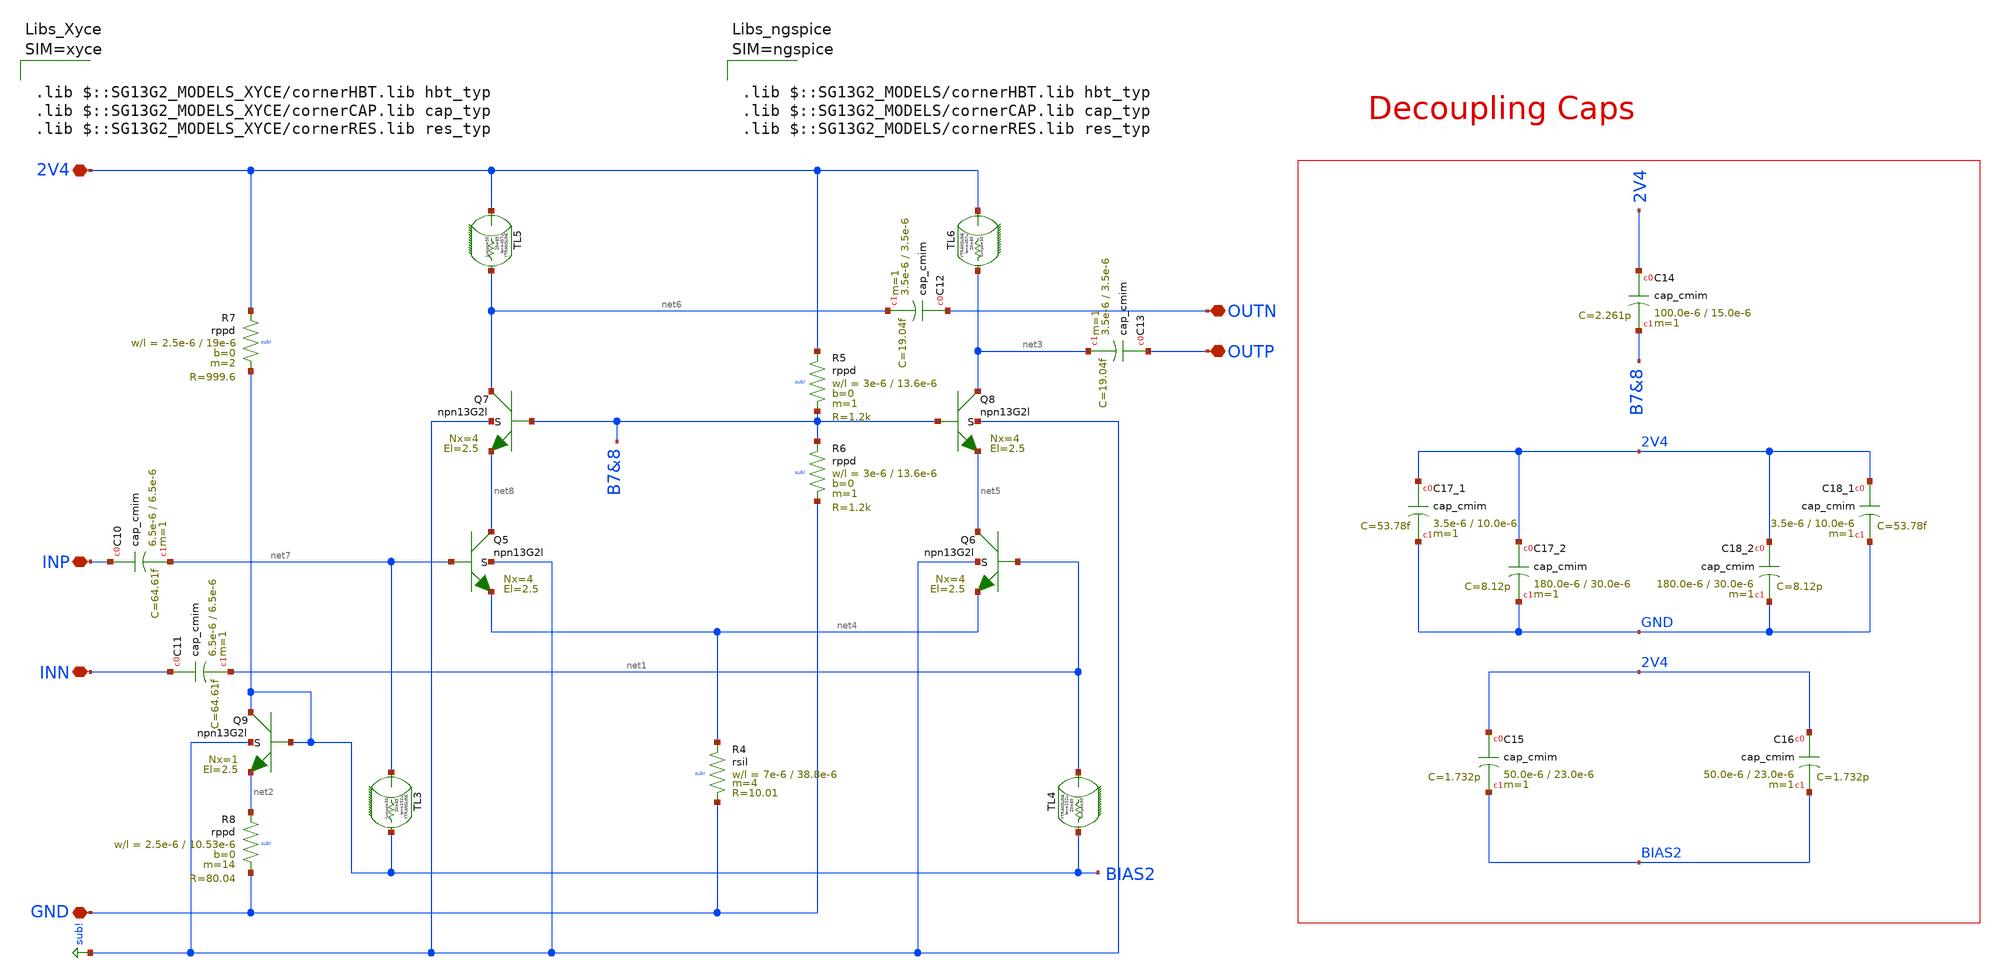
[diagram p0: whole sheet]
** sch_path: mWATTBAT/design_data/xschem/RFAMP_50GD.sch
**.subckt RFAMP_50GD 2V4 GND OUTN OUTP INP INN
*.iopin 2V4
*.iopin GND
*.iopin OUTN
*.iopin OUTP
*.iopin INP
*.iopin INN
XQ5 net8 net7 net4 sub! npn13G2l Nx=4 El=2.5 mm_ok=1
XQ6 net5 net1 net4 sub! npn13G2l Nx=4 El=2.5 mm_ok=1
XQ9 BIAS2 BIAS2 net2 sub! npn13G2l Nx=1 El=2.5 mm_ok=1
XQ7 net6 B7&8 net8 sub! npn13G2l Nx=4 El=2.5 mm_ok=1
XQ8 net3 B7&8 net5 sub! npn13G2l Nx=4 El=2.5 mm_ok=1
ytransline TL5 2V4 net6 ytransline_TL5 len=457u lumps=50
.model ytransline_TL5 transline r=13.18k l=445.8n C=61.5p
ytransline TL6 2V4 net3 ytransline_TL6 len=457u lumps=50
.model ytransline_TL6 transline r=13.18k l=445.8n C=61.5p
ytransline TL3 net7 BIAS2 ytransline_TL3 len=152u lumps=50
.model ytransline_TL3 transline r=13.18k l=445.8n C=61.5p
ytransline TL4 net1 BIAS2 ytransline_TL4 len=152u lumps=50
.model ytransline_TL4 transline r=13.18k l=445.8n C=61.5p
XR7 2V4 BIAS2 sub! rppd w=2.5e-6 l=19e-6 m=2 b=0 mm_ok=1
XC10 INP net7 cap_cmim w=6.5e-6 l=6.5e-6 m=1 mm_ok=1
XC11 INN net1 cap_cmim w=6.5e-6 l=6.5e-6 m=1 mm_ok=1
XC12 OUTN net6 cap_cmim w=3.5e-6 l=3.5e-6 m=1 mm_ok=1
XC13 OUTP net3 cap_cmim w=3.5e-6 l=3.5e-6 m=1 mm_ok=1
XC14 2V4 B7&8 cap_cmim w=100.0e-6 l=15.0e-6 m=1 mm_ok=1
XC15 2V4 BIAS2 cap_cmim w=50.0e-6 l=23.0e-6 m=1 mm_ok=1
XC16 2V4 BIAS2 cap_cmim w=50.0e-6 l=23.0e-6 m=1 mm_ok=1
XC17_1 2V4 GND cap_cmim w=3.5e-6 l=10.0e-6 m=1 mm_ok=1
XC17_2 2V4 GND cap_cmim w=180.0e-6 l=30.0e-6 m=1 mm_ok=1
XC18_1 2V4 GND cap_cmim w=3.5e-6 l=10.0e-6 m=1 mm_ok=1
XC18_2 2V4 GND cap_cmim w=180.0e-6 l=30.0e-6 m=1 mm_ok=1
XR6 B7&8 GND sub! rppd w=3e-6 l=13.6e-6 m=1 b=0 mm_ok=1
XR5 2V4 B7&8 sub! rppd w=3e-6 l=13.6e-6 m=1 b=0 mm_ok=1
XR8 net2 GND sub! rppd w=2.5e-6 l=10.53e-6 m=14 b=0 mm_ok=1
XR4 net4 GND sub! rsil w=7e-6 l=38.8e-6 m=4 mm_ok=1
**** begin user architecture code






.lib $::SG13G2_MODELS/cornerHBT.lib hbt_typ
.lib $::SG13G2_MODELS/cornerCAP.lib cap_typ
.lib $::SG13G2_MODELS/cornerRES.lib res_typ



**** end user architecture code
**.ends
.GLOBAL sub!
.end
